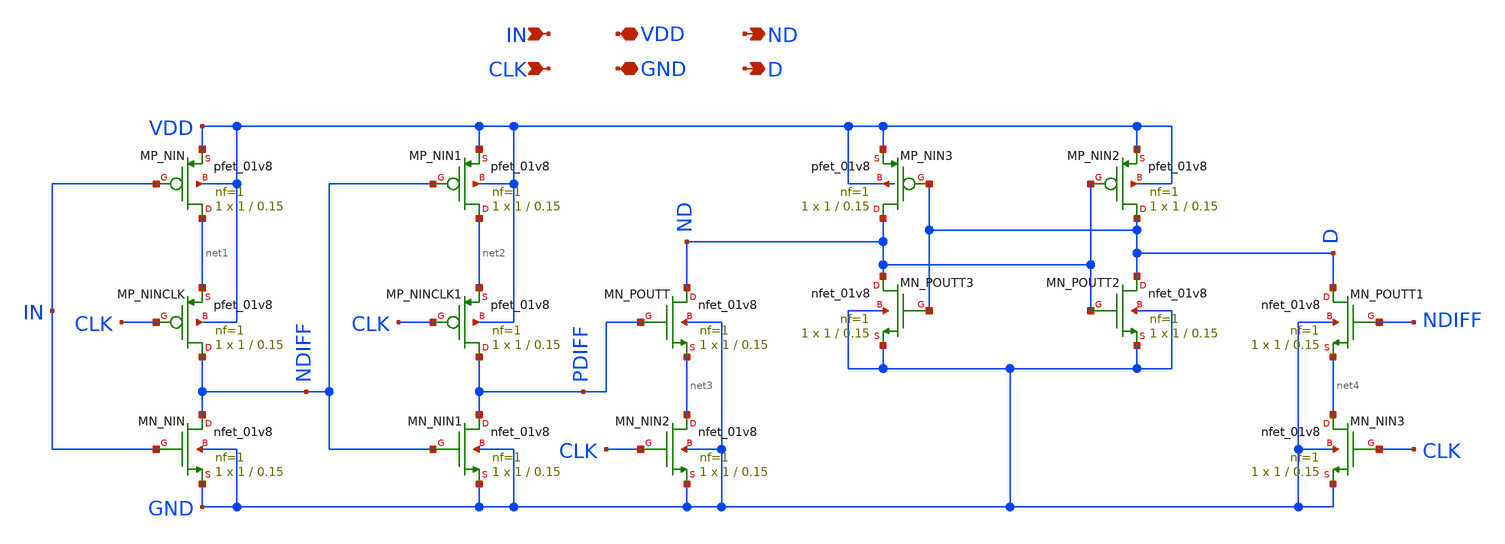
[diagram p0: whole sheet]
** sch_path: samples/cace-tests/SDC/xschem/DFF_v4p1.sch
**.subckt DFF_v4p1 IN CLK VDD GND ND D
*.ipin IN
*.ipin CLK
*.iopin VDD
*.iopin GND
*.opin ND
*.opin D
XMN_NIN NDIFF IN GND GND sky130_fd_pr__nfet_01v8 L=0.15 W=1 nf=1 ad='int((nf+1)/2) * W/nf * 0.29' as='int((nf+2)/2) * W/nf * 0.29'
+ pd='2*int((nf+1)/2) * (W/nf + 0.29)' ps='2*int((nf+2)/2) * (W/nf + 0.29)' nrd='0.29 / W' nrs='0.29 / W'
+ sa=0 sb=0 sd=0 mult=1 m=1
XMP_NINCLK NDIFF CLK net1 VDD sky130_fd_pr__pfet_01v8 L=0.15 W=1 nf=1 ad='int((nf+1)/2) * W/nf * 0.29'
+ as='int((nf+2)/2) * W/nf * 0.29' pd='2*int((nf+1)/2) * (W/nf + 0.29)' ps='2*int((nf+2)/2) * (W/nf + 0.29)'
+ nrd='0.29 / W' nrs='0.29 / W' sa=0 sb=0 sd=0 mult=1 m=1
XMP_NIN net1 IN VDD VDD sky130_fd_pr__pfet_01v8 L=0.15 W=1 nf=1 ad='int((nf+1)/2) * W/nf * 0.29' as='int((nf+2)/2) * W/nf * 0.29'
+ pd='2*int((nf+1)/2) * (W/nf + 0.29)' ps='2*int((nf+2)/2) * (W/nf + 0.29)' nrd='0.29 / W' nrs='0.29 / W'
+ sa=0 sb=0 sd=0 mult=1 m=1
XMN_NIN1 PDIFF NDIFF GND GND sky130_fd_pr__nfet_01v8 L=0.15 W=1 nf=1 ad='int((nf+1)/2) * W/nf * 0.29'
+ as='int((nf+2)/2) * W/nf * 0.29' pd='2*int((nf+1)/2) * (W/nf + 0.29)' ps='2*int((nf+2)/2) * (W/nf + 0.29)'
+ nrd='0.29 / W' nrs='0.29 / W' sa=0 sb=0 sd=0 mult=1 m=1
XMP_NINCLK1 PDIFF CLK net2 VDD sky130_fd_pr__pfet_01v8 L=0.15 W=1 nf=1 ad='int((nf+1)/2) * W/nf * 0.29'
+ as='int((nf+2)/2) * W/nf * 0.29' pd='2*int((nf+1)/2) * (W/nf + 0.29)' ps='2*int((nf+2)/2) * (W/nf + 0.29)'
+ nrd='0.29 / W' nrs='0.29 / W' sa=0 sb=0 sd=0 mult=1 m=1
XMP_NIN1 net2 NDIFF VDD VDD sky130_fd_pr__pfet_01v8 L=0.15 W=1 nf=1 ad='int((nf+1)/2) * W/nf * 0.29'
+ as='int((nf+2)/2) * W/nf * 0.29' pd='2*int((nf+1)/2) * (W/nf + 0.29)' ps='2*int((nf+2)/2) * (W/nf + 0.29)'
+ nrd='0.29 / W' nrs='0.29 / W' sa=0 sb=0 sd=0 mult=1 m=1
XMN_NIN2 net3 CLK GND GND sky130_fd_pr__nfet_01v8 L=0.15 W=1 nf=1 ad='int((nf+1)/2) * W/nf * 0.29' as='int((nf+2)/2) * W/nf * 0.29'
+ pd='2*int((nf+1)/2) * (W/nf + 0.29)' ps='2*int((nf+2)/2) * (W/nf + 0.29)' nrd='0.29 / W' nrs='0.29 / W'
+ sa=0 sb=0 sd=0 mult=1 m=1
XMN_POUTT ND PDIFF net3 GND sky130_fd_pr__nfet_01v8 L=0.15 W=1 nf=1 ad='int((nf+1)/2) * W/nf * 0.29'
+ as='int((nf+2)/2) * W/nf * 0.29' pd='2*int((nf+1)/2) * (W/nf + 0.29)' ps='2*int((nf+2)/2) * (W/nf + 0.29)'
+ nrd='0.29 / W' nrs='0.29 / W' sa=0 sb=0 sd=0 mult=1 m=1
XMN_POUTT1 D NDIFF net4 GND sky130_fd_pr__nfet_01v8 L=0.15 W=1 nf=1 ad='int((nf+1)/2) * W/nf * 0.29'
+ as='int((nf+2)/2) * W/nf * 0.29' pd='2*int((nf+1)/2) * (W/nf + 0.29)' ps='2*int((nf+2)/2) * (W/nf + 0.29)'
+ nrd='0.29 / W' nrs='0.29 / W' sa=0 sb=0 sd=0 mult=1 m=1
XMN_POUTT2 D ND GND GND sky130_fd_pr__nfet_01v8 L=0.15 W=1 nf=1 ad='int((nf+1)/2) * W/nf * 0.29' as='int((nf+2)/2) * W/nf * 0.29'
+ pd='2*int((nf+1)/2) * (W/nf + 0.29)' ps='2*int((nf+2)/2) * (W/nf + 0.29)' nrd='0.29 / W' nrs='0.29 / W'
+ sa=0 sb=0 sd=0 mult=1 m=1
XMP_NIN2 D ND VDD VDD sky130_fd_pr__pfet_01v8 L=0.15 W=1 nf=1 ad='int((nf+1)/2) * W/nf * 0.29' as='int((nf+2)/2) * W/nf * 0.29'
+ pd='2*int((nf+1)/2) * (W/nf + 0.29)' ps='2*int((nf+2)/2) * (W/nf + 0.29)' nrd='0.29 / W' nrs='0.29 / W'
+ sa=0 sb=0 sd=0 mult=1 m=1
XMN_POUTT3 ND D GND GND sky130_fd_pr__nfet_01v8 L=0.15 W=1 nf=1 ad='int((nf+1)/2) * W/nf * 0.29' as='int((nf+2)/2) * W/nf * 0.29'
+ pd='2*int((nf+1)/2) * (W/nf + 0.29)' ps='2*int((nf+2)/2) * (W/nf + 0.29)' nrd='0.29 / W' nrs='0.29 / W'
+ sa=0 sb=0 sd=0 mult=1 m=1
XMP_NIN3 ND D VDD VDD sky130_fd_pr__pfet_01v8 L=0.15 W=1 nf=1 ad='int((nf+1)/2) * W/nf * 0.29' as='int((nf+2)/2) * W/nf * 0.29'
+ pd='2*int((nf+1)/2) * (W/nf + 0.29)' ps='2*int((nf+2)/2) * (W/nf + 0.29)' nrd='0.29 / W' nrs='0.29 / W'
+ sa=0 sb=0 sd=0 mult=1 m=1
XMN_NIN3 net4 CLK GND GND sky130_fd_pr__nfet_01v8 L=0.15 W=1 nf=1 ad='int((nf+1)/2) * W/nf * 0.29' as='int((nf+2)/2) * W/nf * 0.29'
+ pd='2*int((nf+1)/2) * (W/nf + 0.29)' ps='2*int((nf+2)/2) * (W/nf + 0.29)' nrd='0.29 / W' nrs='0.29 / W'
+ sa=0 sb=0 sd=0 mult=1 m=1
**.ends
.end
